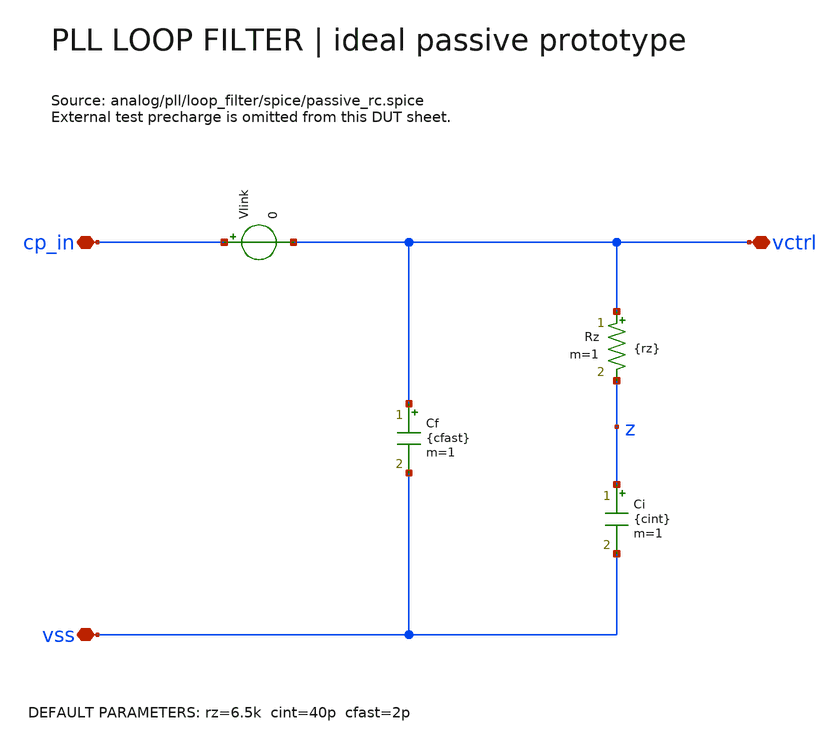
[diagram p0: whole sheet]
** sch_path: analog/pll/loop_filter/schematic/pll_loop_filter.sch
**.subckt pll_loop_filter cp_in vctrl vss
*.iopin cp_in
*.iopin vctrl
*.iopin vss
Vlink cp_in vctrl 0
Cf vctrl vss {cfast} m=1
Rz vctrl z {rz} m=1
Ci z vss {cint} m=1
**.ends
.end
